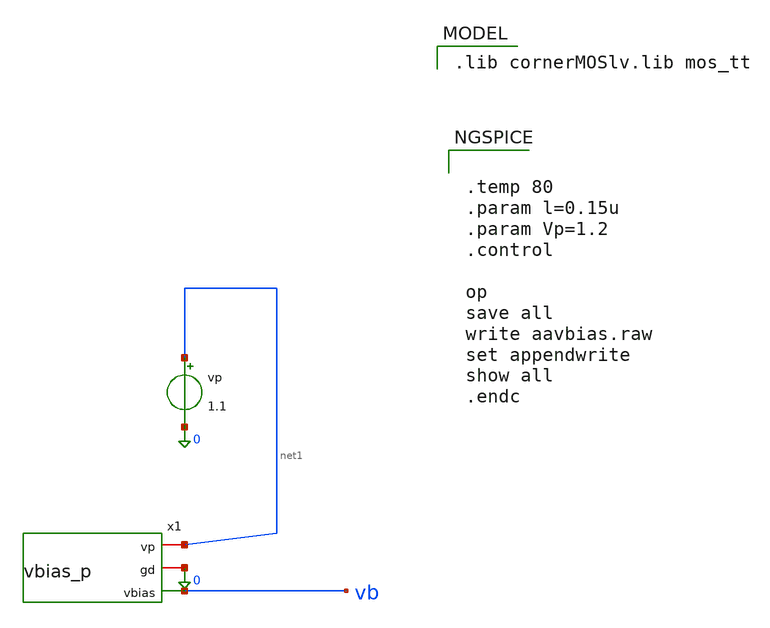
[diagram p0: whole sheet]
** sch_path: schematics/charge_pump/vbias_n_tb.sch
**.subckt vbias_n_tb
vp net1 0 1.1
x1 net1 0 vb vbias_p
**** begin user architecture code
 .lib cornerMOSlv.lib mos_tt



.temp 80
.param l=0.15u
.param Vp=1.2
.control

op
save all
write aavbias.raw
set appendwrite
show all
.endc


**** end user architecture code
**.ends
.end
